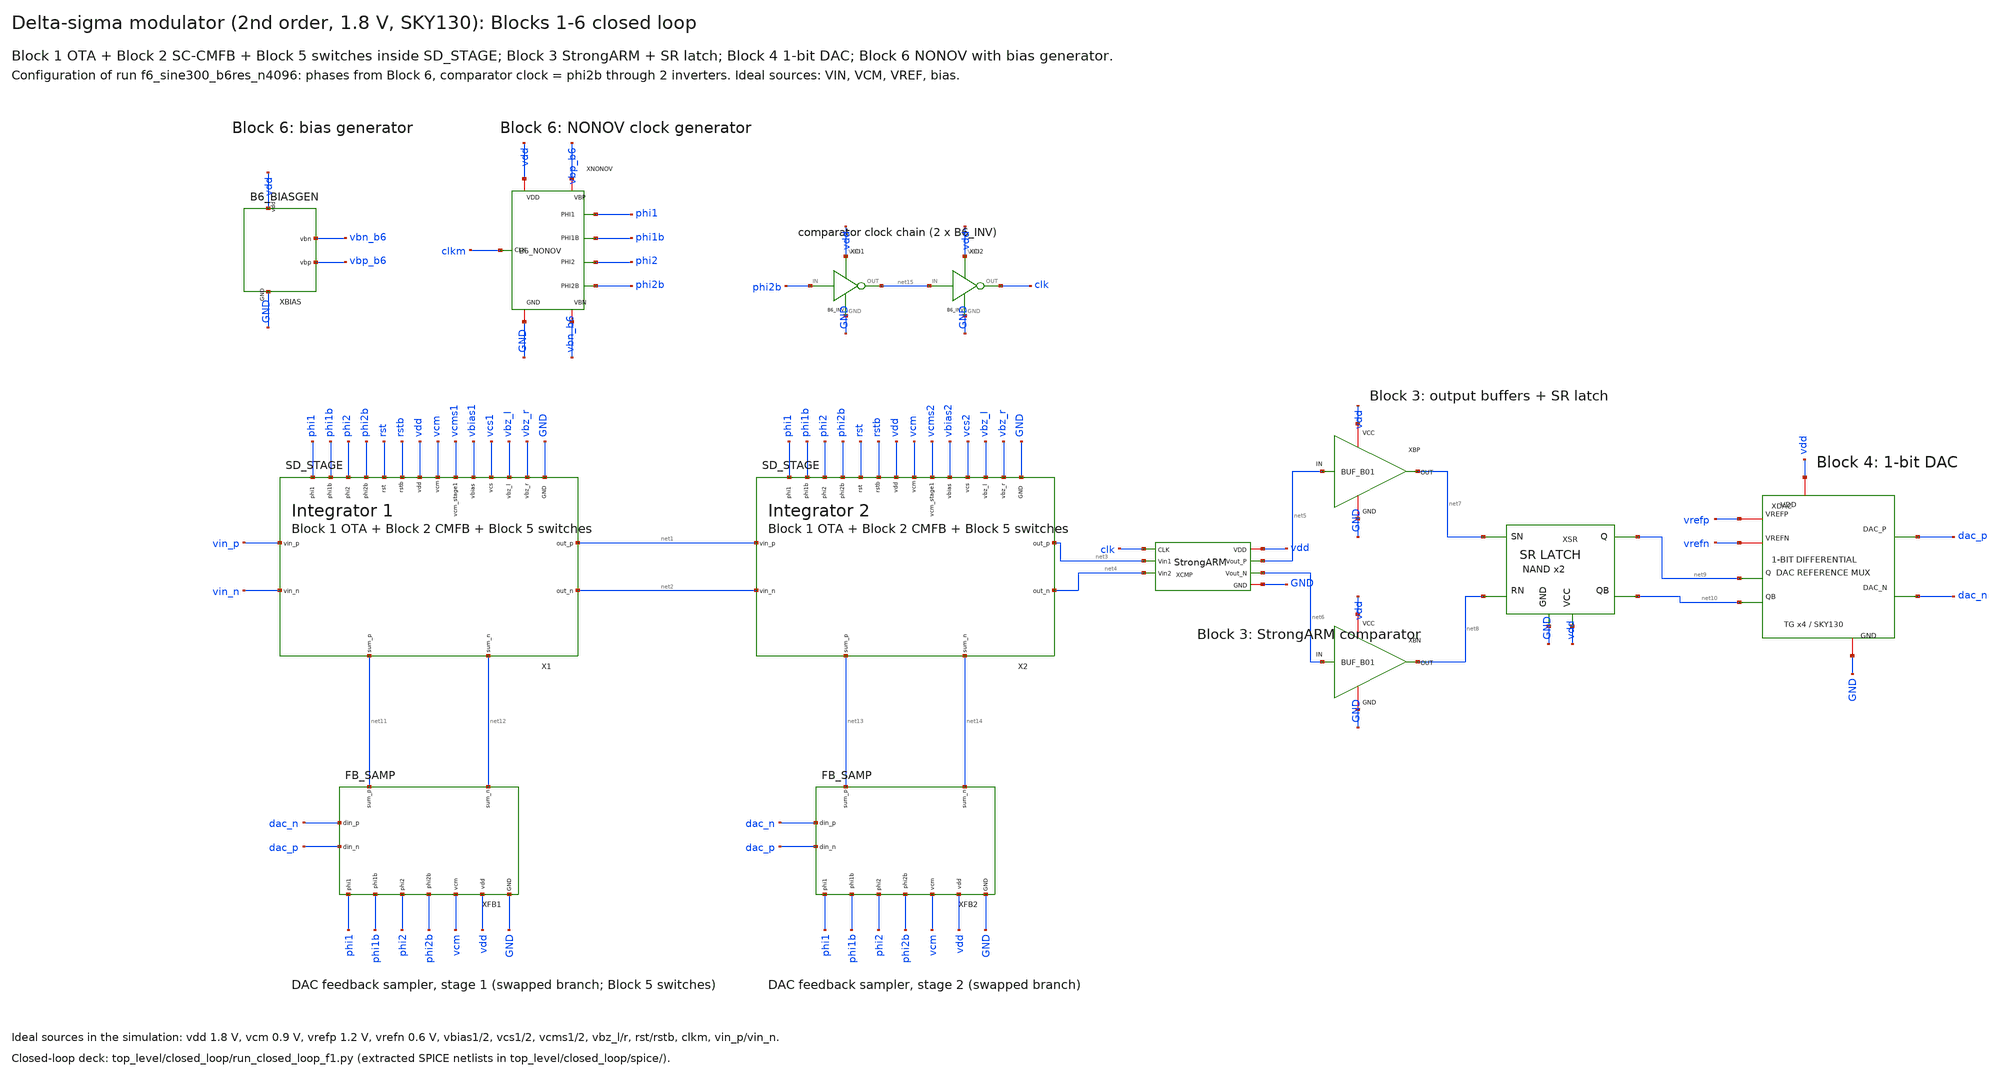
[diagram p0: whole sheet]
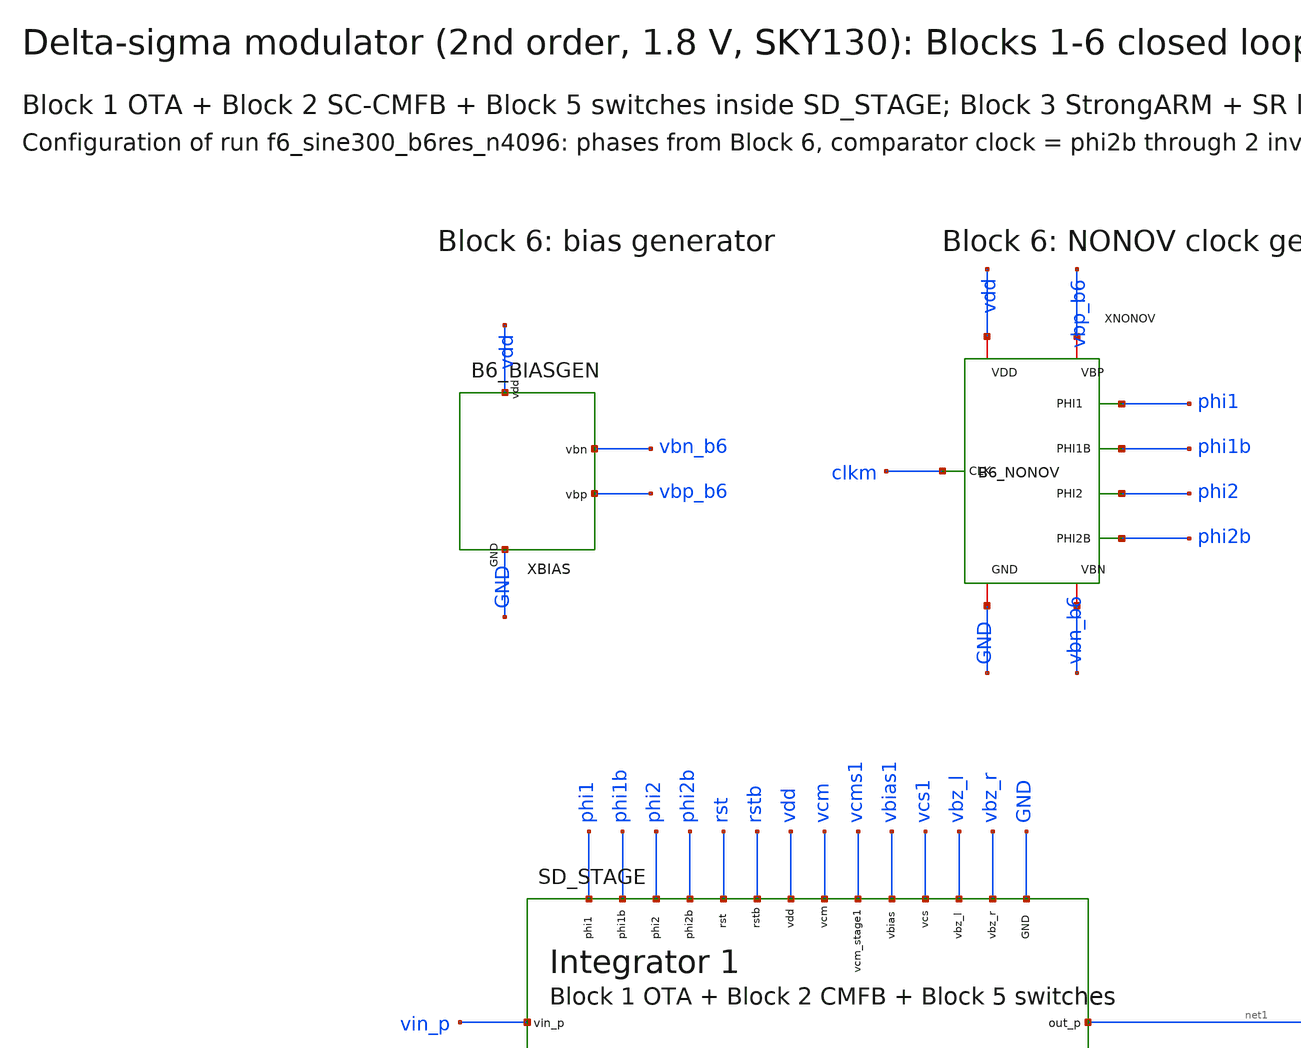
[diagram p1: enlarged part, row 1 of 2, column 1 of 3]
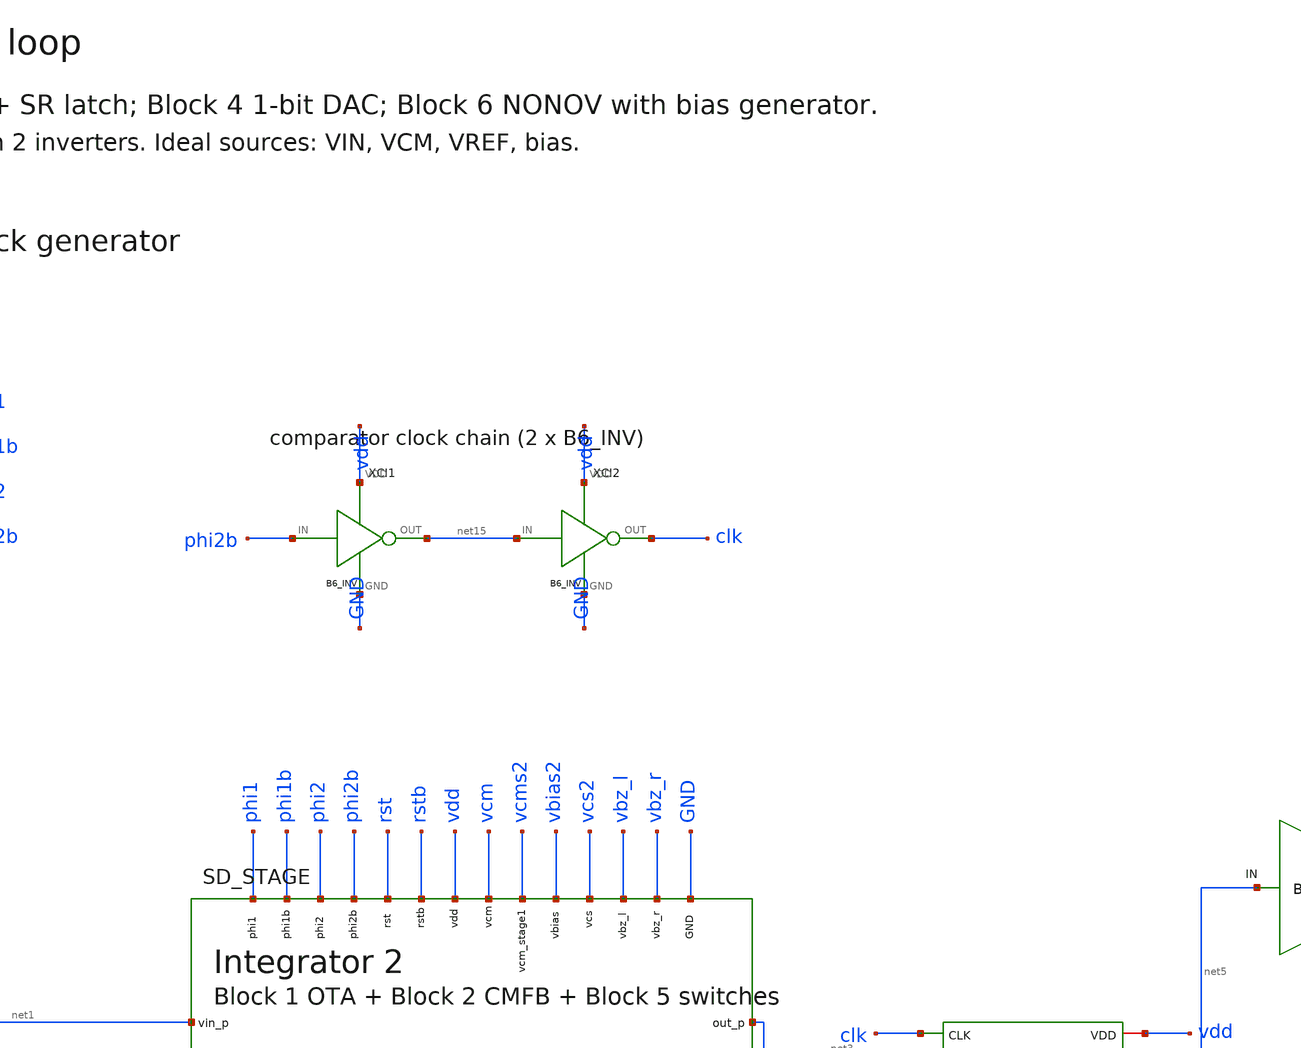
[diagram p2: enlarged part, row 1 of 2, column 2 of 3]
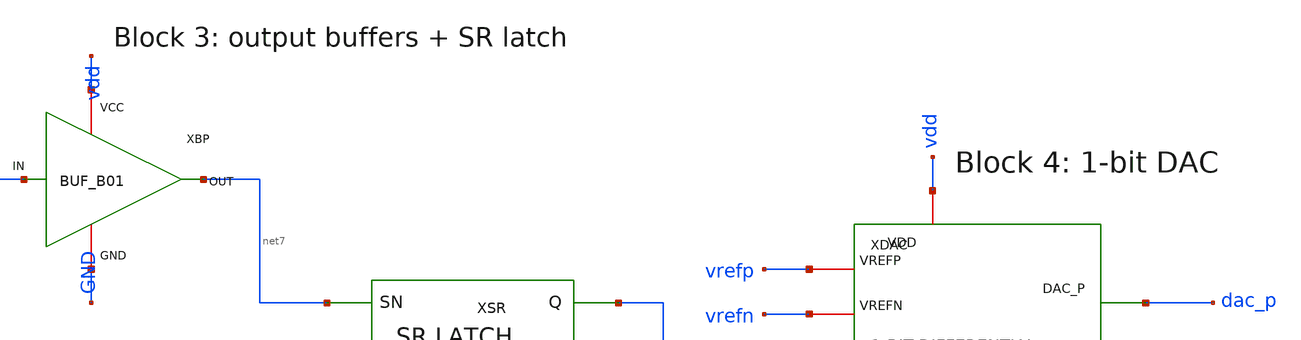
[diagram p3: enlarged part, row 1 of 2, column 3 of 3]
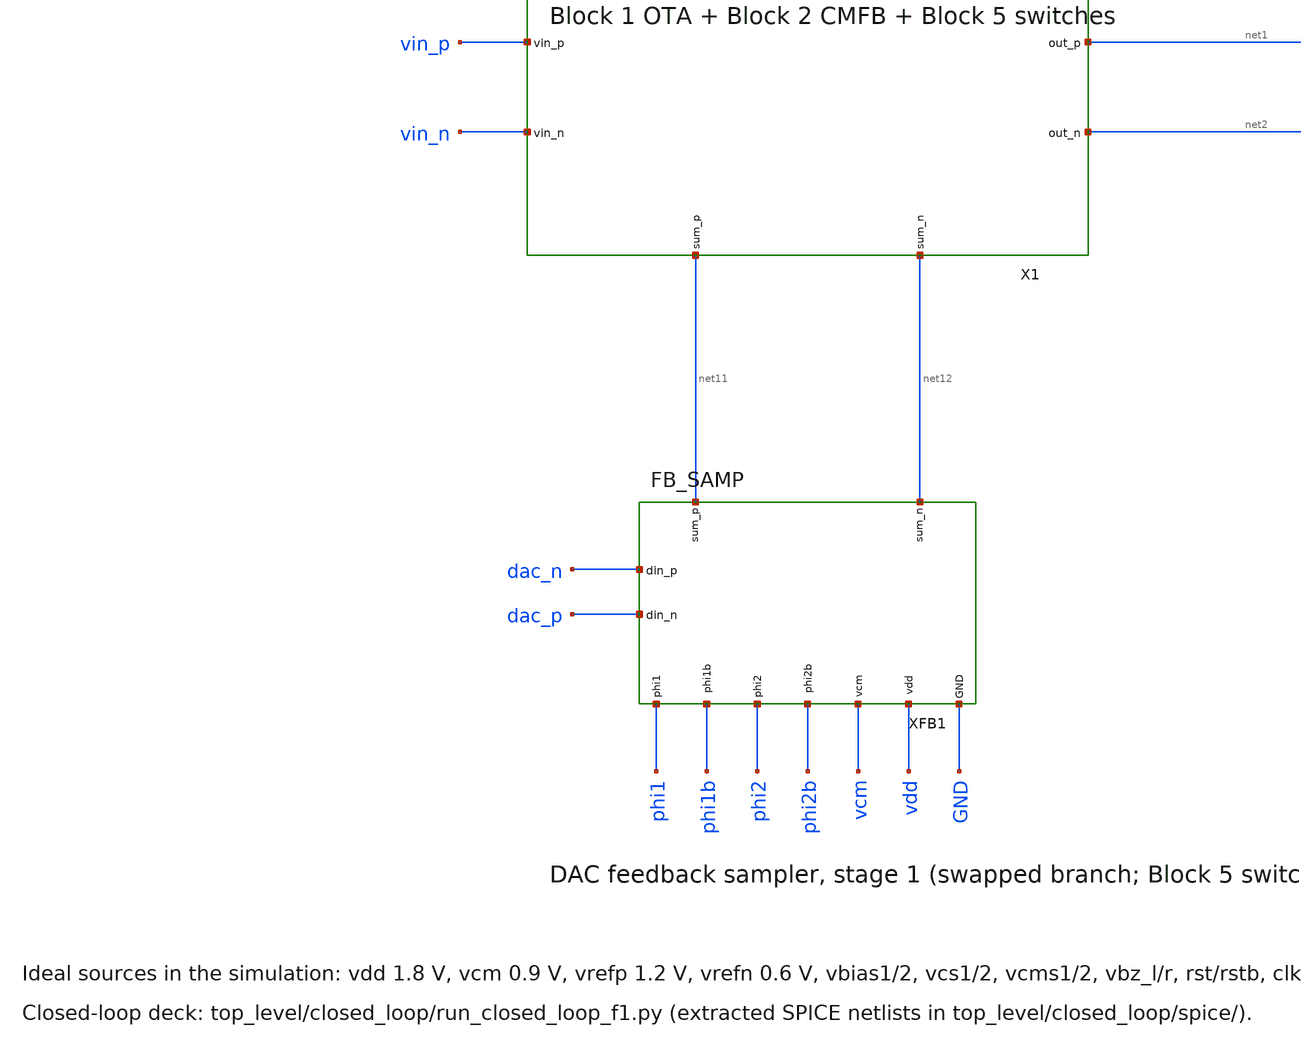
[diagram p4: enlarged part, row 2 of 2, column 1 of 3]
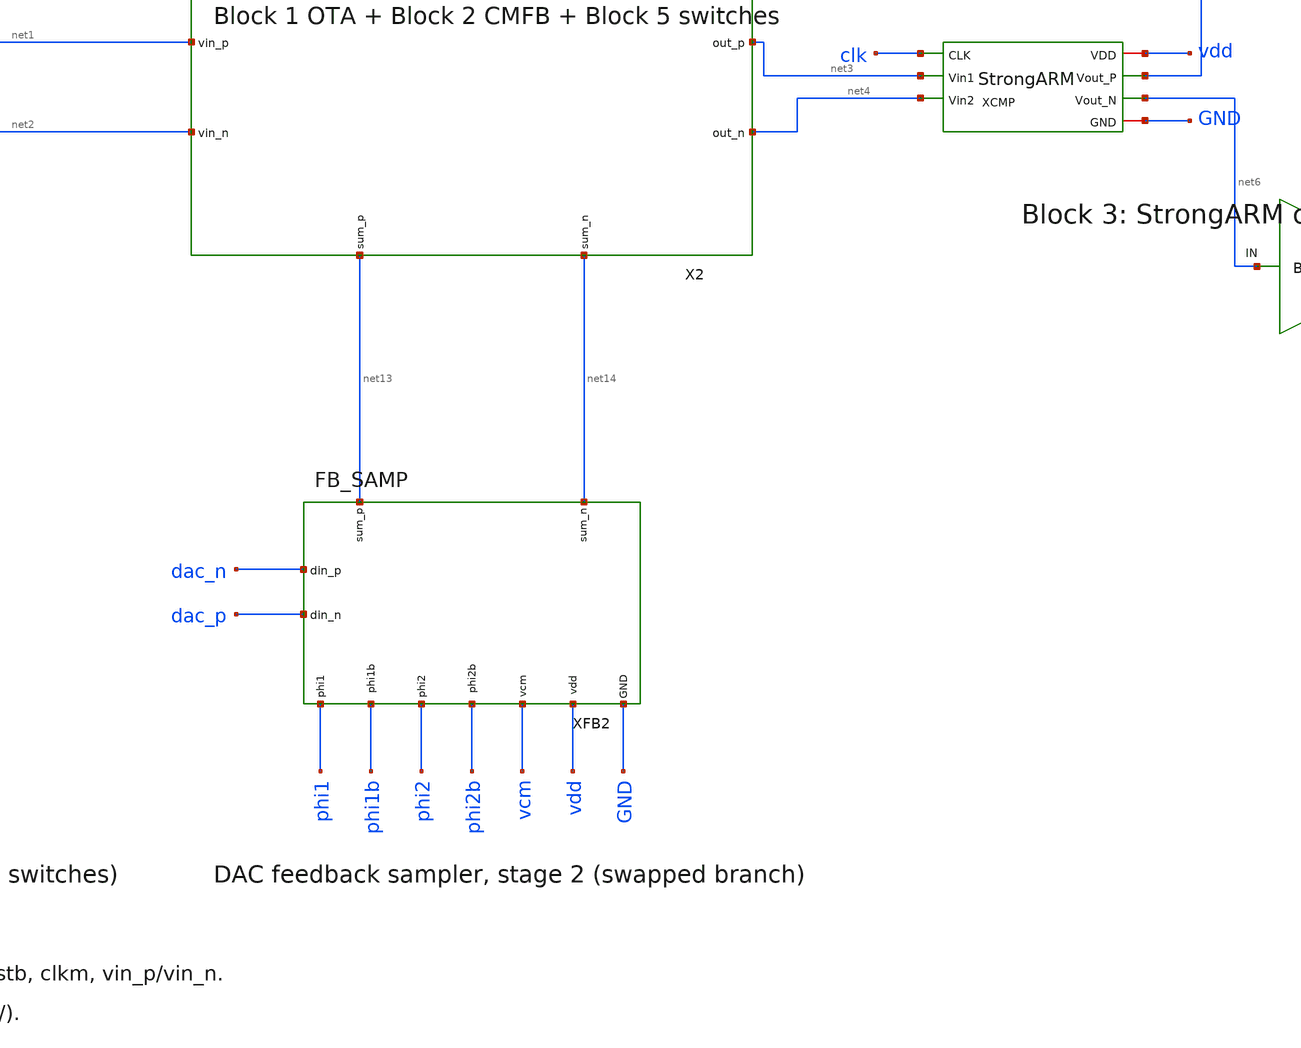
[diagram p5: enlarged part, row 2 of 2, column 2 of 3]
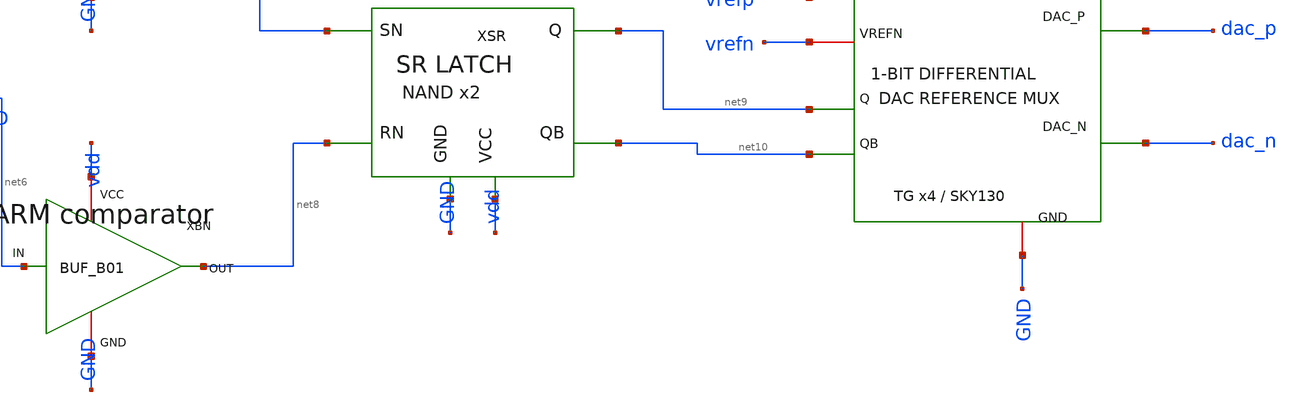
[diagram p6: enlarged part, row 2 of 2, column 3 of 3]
** sch_path: top_level/xschem/SD_TOP.sch
**.subckt SD_TOP
X1 vin_p vin_n net1 net2 net11 net12 phi1 phi1b phi2 phi2b rst rstb vdd vcm vcms1 vbias1 vcs1 vbz_l
+ vbz_r GND SD_STAGE
X2 net1 net2 net3 net4 net13 net14 phi1 phi1b phi2 phi2b rst rstb vdd vcm vcms2 vbias2 vcs2 vbz_l
+ vbz_r GND SD_STAGE
XCMP vdd clk net5 net6 net3 net4 GND StrongARM
XBP vdd net5 net7 GND BUF_B01
XBN vdd net6 net8 GND BUF_B01
XSR net7 net8 net9 net10 GND vdd SR_Latch
XDAC vrefp vrefn net9 net10 vdd GND dac_p dac_n DAC_1bit
XFB1 dac_n dac_p net11 net12 phi1 phi1b phi2 phi2b vcm vdd GND FB_SAMP
XFB2 dac_n dac_p net13 net14 phi1 phi1b phi2 phi2b vcm vdd GND FB_SAMP
XNONOV clkm phi1 phi1b phi2 phi2b vdd vbp_b6 GND vbn_b6 B6_NONOV
XBIAS vdd GND vbn_b6 vbp_b6 B6_BIASGEN
XCI1 phi2b net15 vdd GND B6_INV
XCI2 net15 clk vdd GND B6_INV
**.ends
.end
